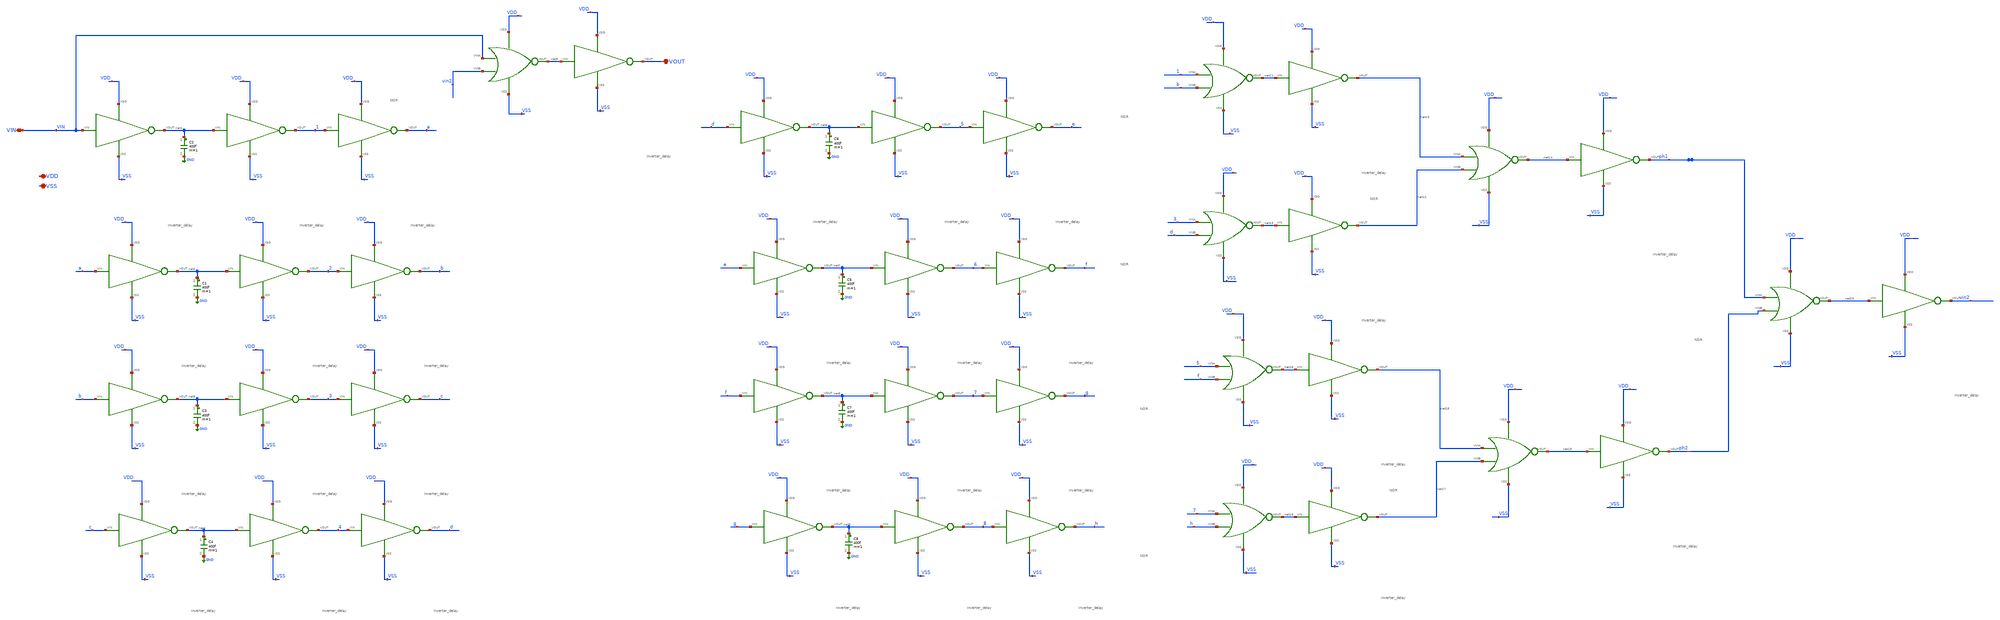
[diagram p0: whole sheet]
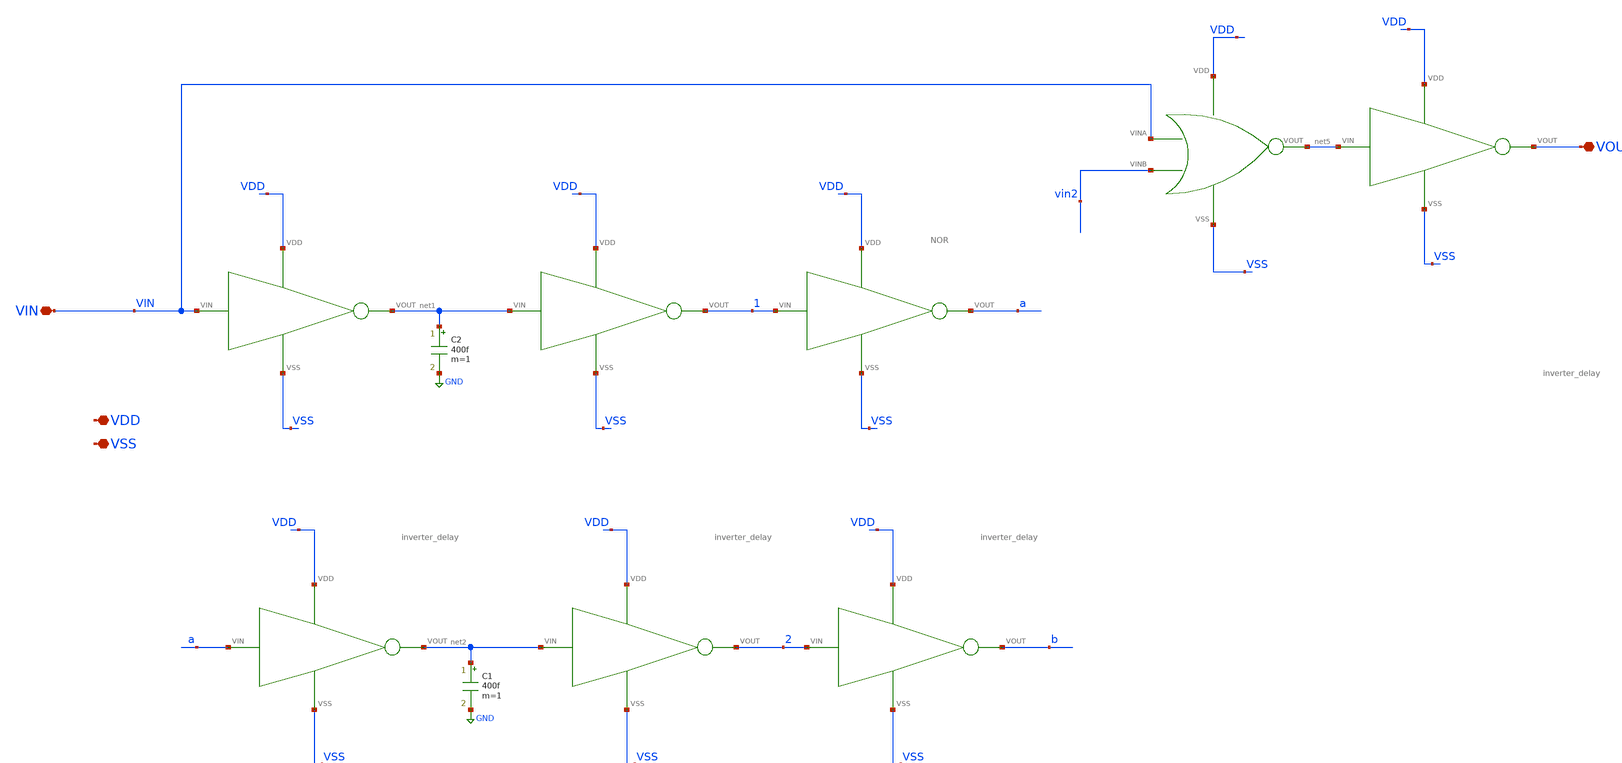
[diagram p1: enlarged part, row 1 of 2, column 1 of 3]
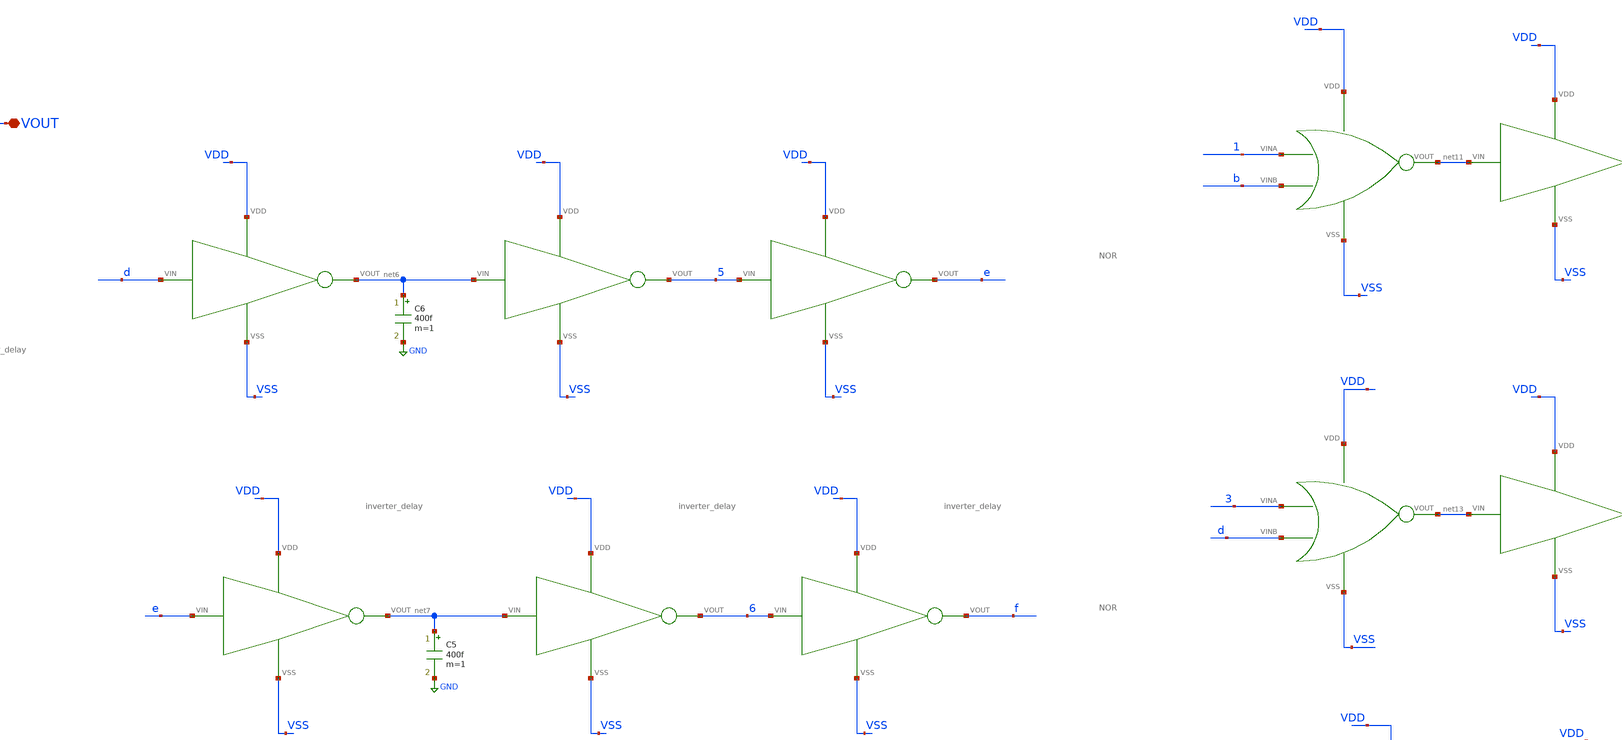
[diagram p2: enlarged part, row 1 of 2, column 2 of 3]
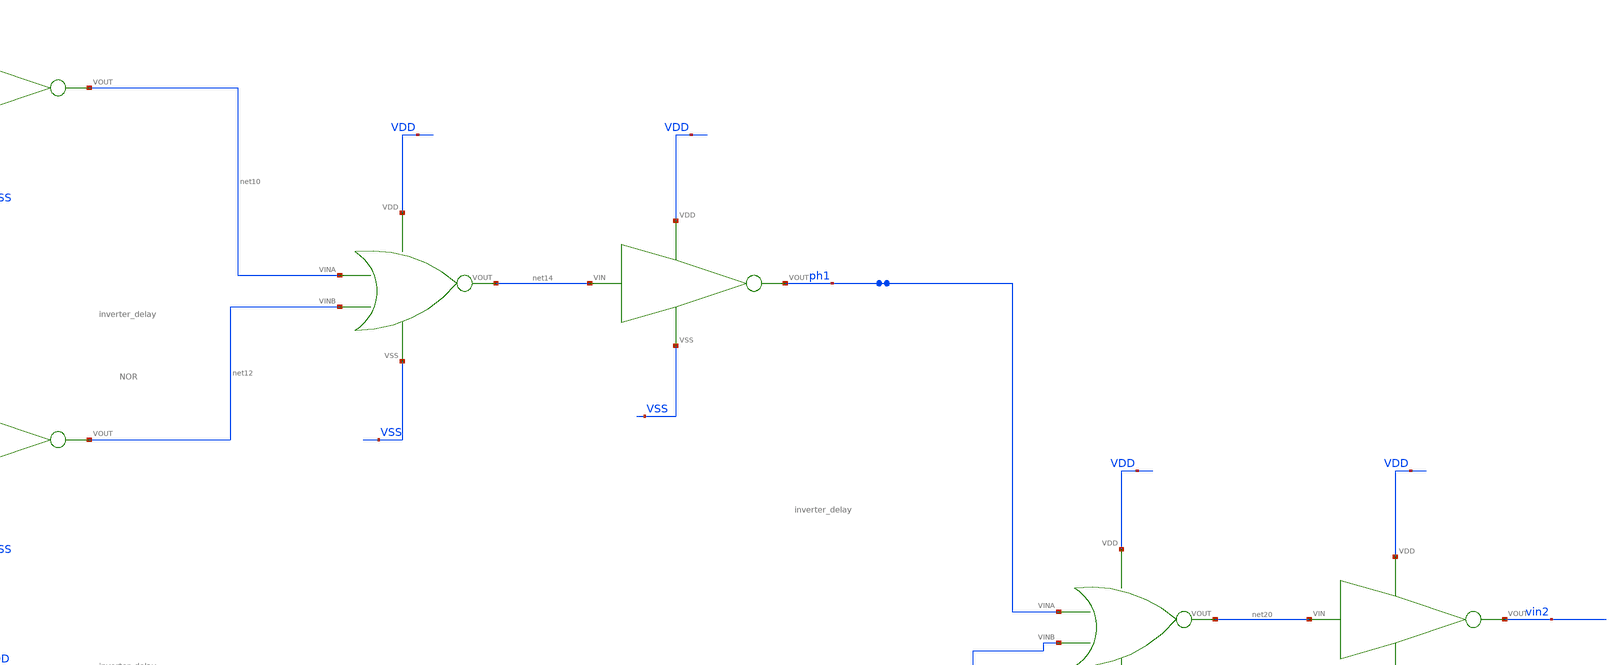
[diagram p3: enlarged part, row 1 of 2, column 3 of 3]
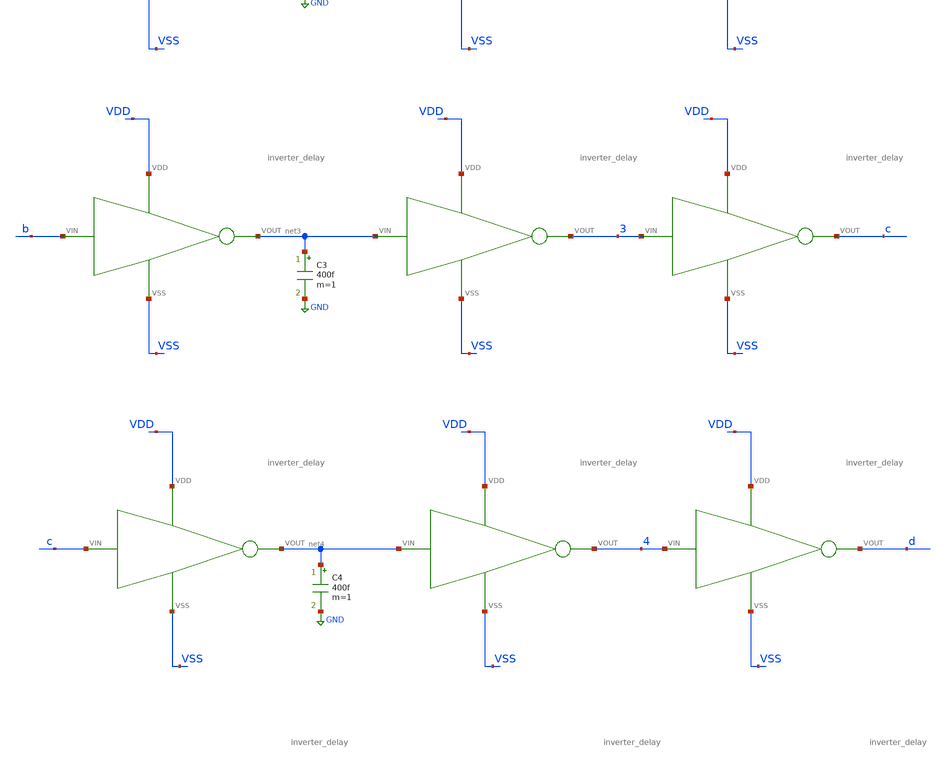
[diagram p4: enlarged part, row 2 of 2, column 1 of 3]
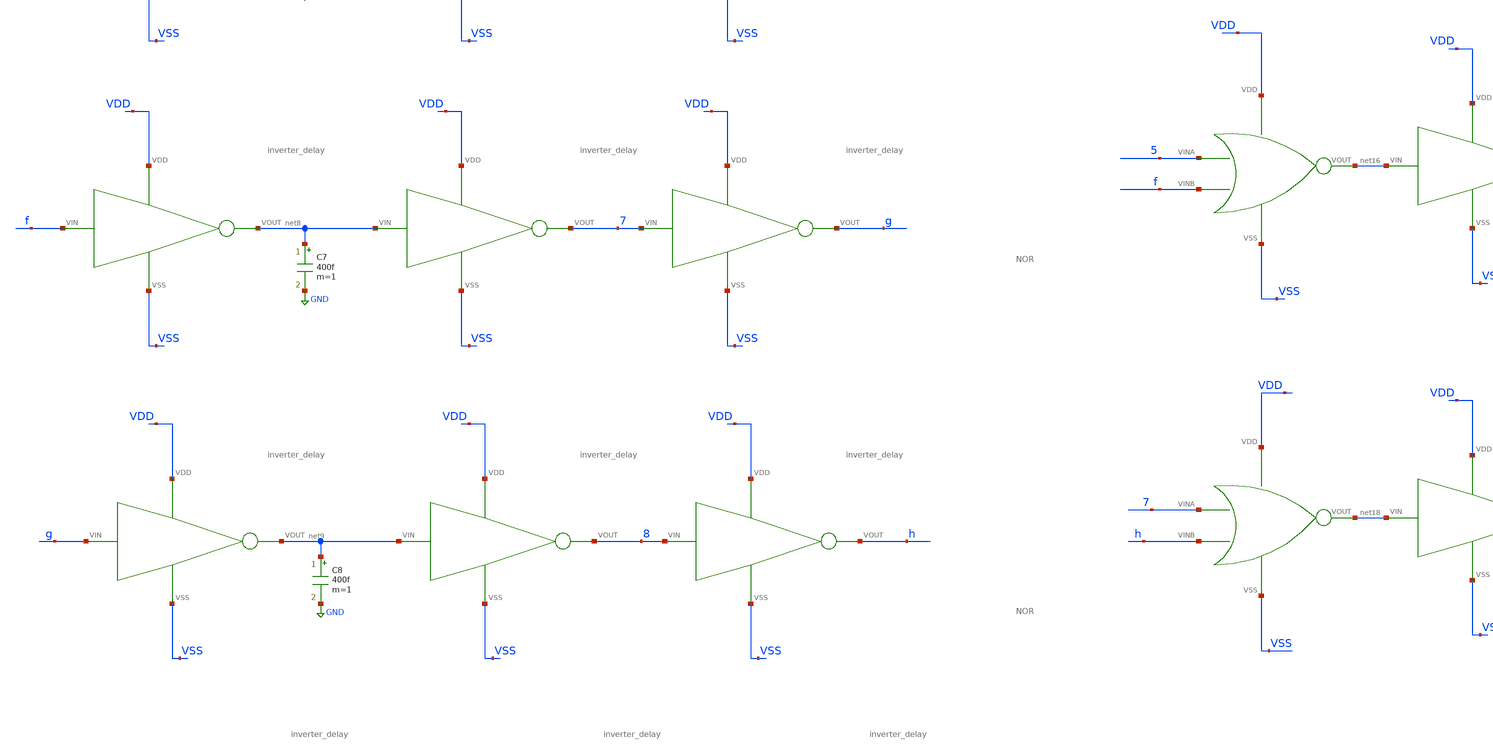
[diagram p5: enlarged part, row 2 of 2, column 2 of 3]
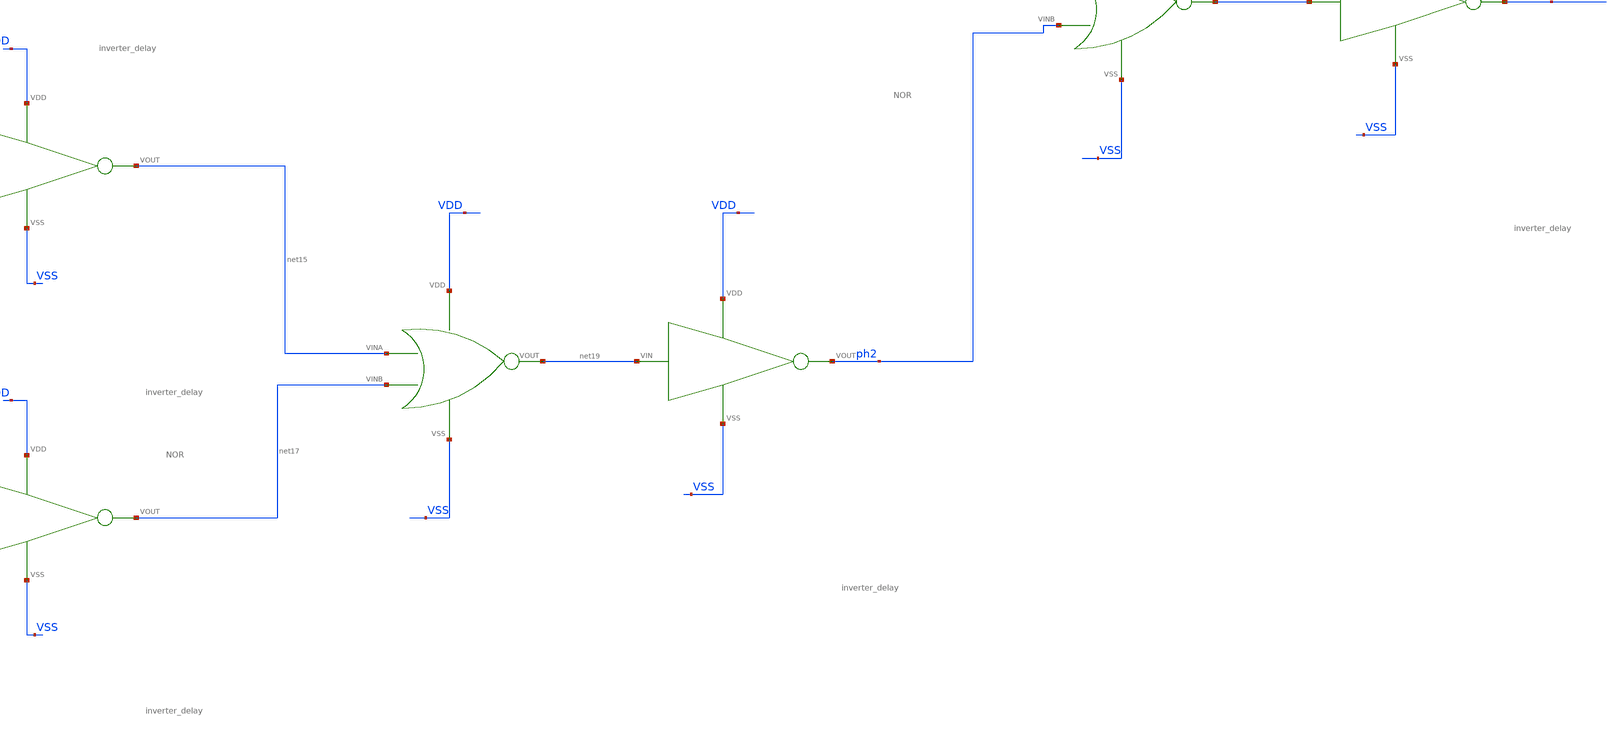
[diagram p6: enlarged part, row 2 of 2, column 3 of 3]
** sch_path: xschem/DC_DC_Converter_xschem/OTHERS/DC_DC_Converter_JV11/Inverter/delay_block_with_less_delay_for_symbol.sch
**.subckt delay_block_with_less_delay_for_symbol VDD VSS VIN VOUT
*.iopin VDD
*.iopin VSS
*.iopin VIN
*.iopin VOUT
X1 net1 VIN VDD VSS inverter_delay
X2 1 net1 VDD VSS inverter_delay
X3 a 1 VDD VSS inverter_delay
X4 net2 a VDD VSS inverter_delay
X5 2 net2 VDD VSS inverter_delay
X6 b 2 VDD VSS inverter_delay
X7 net3 b VDD VSS inverter_delay
X8 3 net3 VDD VSS inverter_delay
X9 c 3 VDD VSS inverter_delay
X10 net4 c VDD VSS inverter_delay
X11 4 net4 VDD VSS inverter_delay
X12 d 4 VDD VSS inverter_delay
X13 VOUT net5 VDD VSS inverter_delay
C1 net2 GND 400f m=1
C2 net1 GND 400f m=1
C3 net3 GND 400f m=1
C4 net4 GND 400f m=1
X14 net6 d VDD VSS inverter_delay
X15 5 net6 VDD VSS inverter_delay
X16 e 5 VDD VSS inverter_delay
X17 net7 e VDD VSS inverter_delay
X18 6 net7 VDD VSS inverter_delay
X19 f 6 VDD VSS inverter_delay
X20 net8 f VDD VSS inverter_delay
X21 7 net8 VDD VSS inverter_delay
X22 g 7 VDD VSS inverter_delay
X23 net9 g VDD VSS inverter_delay
X24 8 net9 VDD VSS inverter_delay
X25 h 8 VDD VSS inverter_delay
C5 net7 GND 400f m=1
C6 net6 GND 400f m=1
C7 net8 GND 400f m=1
C8 net9 GND 400f m=1
X50 net10 net11 VDD VSS inverter_delay
X51 net12 net13 VDD VSS inverter_delay
X52 ph1 net14 VDD VSS inverter_delay
X53 net15 net16 VDD VSS inverter_delay
X54 net17 net18 VDD VSS inverter_delay
X55 ph2 net19 VDD VSS inverter_delay
X58 vin2 net20 VDD VSS inverter_delay
X62 net5 VIN VDD VSS vin2 NOR
X63 net11 1 VDD VSS b NOR
X64 net13 3 VDD VSS d NOR
X65 net14 net10 VDD VSS net12 NOR
X66 net16 5 VDD VSS f NOR
X67 net18 7 VDD VSS h NOR
X68 net19 net15 VDD VSS net17 NOR
X71 net20 ph1 VDD VSS ph2 NOR
**.ends

* expanding   symbol:  inverter_delay.sym # of pins=4
** sym_path: xschem/DC_DC_Converter_xschem/OTHERS/DC_DC_Converter_JV11/Delay_block_revised/inverter_delay.sym
** sch_path: xschem/DC_DC_Converter_xschem/OTHERS/DC_DC_Converter_JV11/Delay_block_revised/inverter_delay.sch
.subckt inverter_delay VOUT VIN VDD VSS
*.iopin VDD
*.iopin VOUT
*.iopin VSS
*.iopin VIN
XM1 VOUT VIN VSS VSS sky130_fd_pr__nfet_01v8 L=0.15 W=1 nf=1 ad='int((nf+1)/2) * W/nf * 0.29' as='int((nf+2)/2) * W/nf * 0.29'
+ pd='2*int((nf+1)/2) * (W/nf + 0.29)' ps='2*int((nf+2)/2) * (W/nf + 0.29)' nrd='0.29 / W' nrs='0.29 / W'
+ sa=0 sb=0 sd=0 mult=1 m=1
XM2 VOUT VIN VDD VDD sky130_fd_pr__pfet_01v8 L=0.15 W=3 nf=1 ad='int((nf+1)/2) * W/nf * 0.29' as='int((nf+2)/2) * W/nf * 0.29'
+ pd='2*int((nf+1)/2) * (W/nf + 0.29)' ps='2*int((nf+2)/2) * (W/nf + 0.29)' nrd='0.29 / W' nrs='0.29 / W'
+ sa=0 sb=0 sd=0 mult=1 m=1
.ends


* expanding   symbol:  NOR.sym # of pins=5
** sym_path: xschem/DC_DC_Converter_xschem/OTHERS/DC_DC_Converter_6/Delay_block_revised/NOR.sym
** sch_path: xschem/DC_DC_Converter_xschem/OTHERS/DC_DC_Converter_6/Delay_block_revised/NOR.sch
.subckt NOR VOUT VINA VDD VSS VINB
*.iopin VDD
*.iopin VSS
*.iopin VINB
*.iopin VINA
*.iopin VOUT
XM1 VOUT VINB VSS VSS sky130_fd_pr__nfet_01v8 L=0.15 W=200 nf=10 ad='int((nf+1)/2) * W/nf * 0.29' as='int((nf+2)/2) * W/nf * 0.29'
+ pd='2*int((nf+1)/2) * (W/nf + 0.29)' ps='2*int((nf+2)/2) * (W/nf + 0.29)' nrd='0.29 / W' nrs='0.29 / W'
+ sa=0 sb=0 sd=0 mult=1 m=1
XM2 VOUT VINB net1 VDD sky130_fd_pr__pfet_01v8 L=0.15 W=600 nf=20 ad='int((nf+1)/2) * W/nf * 0.29' as='int((nf+2)/2) * W/nf * 0.29'
+ pd='2*int((nf+1)/2) * (W/nf + 0.29)' ps='2*int((nf+2)/2) * (W/nf + 0.29)' nrd='0.29 / W' nrs='0.29 / W'
+ sa=0 sb=0 sd=0 mult=1 m=1
XM3 net1 VINA VDD VDD sky130_fd_pr__pfet_01v8 L=0.15 W=600 nf=20 ad='int((nf+1)/2) * W/nf * 0.29' as='int((nf+2)/2) * W/nf * 0.29'
+ pd='2*int((nf+1)/2) * (W/nf + 0.29)' ps='2*int((nf+2)/2) * (W/nf + 0.29)' nrd='0.29 / W' nrs='0.29 / W'
+ sa=0 sb=0 sd=0 mult=1 m=1
XM4 VOUT VINA VSS VSS sky130_fd_pr__nfet_01v8 L=0.15 W=200 nf=10 ad='int((nf+1)/2) * W/nf * 0.29' as='int((nf+2)/2) * W/nf * 0.29'
+ pd='2*int((nf+1)/2) * (W/nf + 0.29)' ps='2*int((nf+2)/2) * (W/nf + 0.29)' nrd='0.29 / W' nrs='0.29 / W'
+ sa=0 sb=0 sd=0 mult=1 m=1
.ends

.GLOBAL GND
.end
